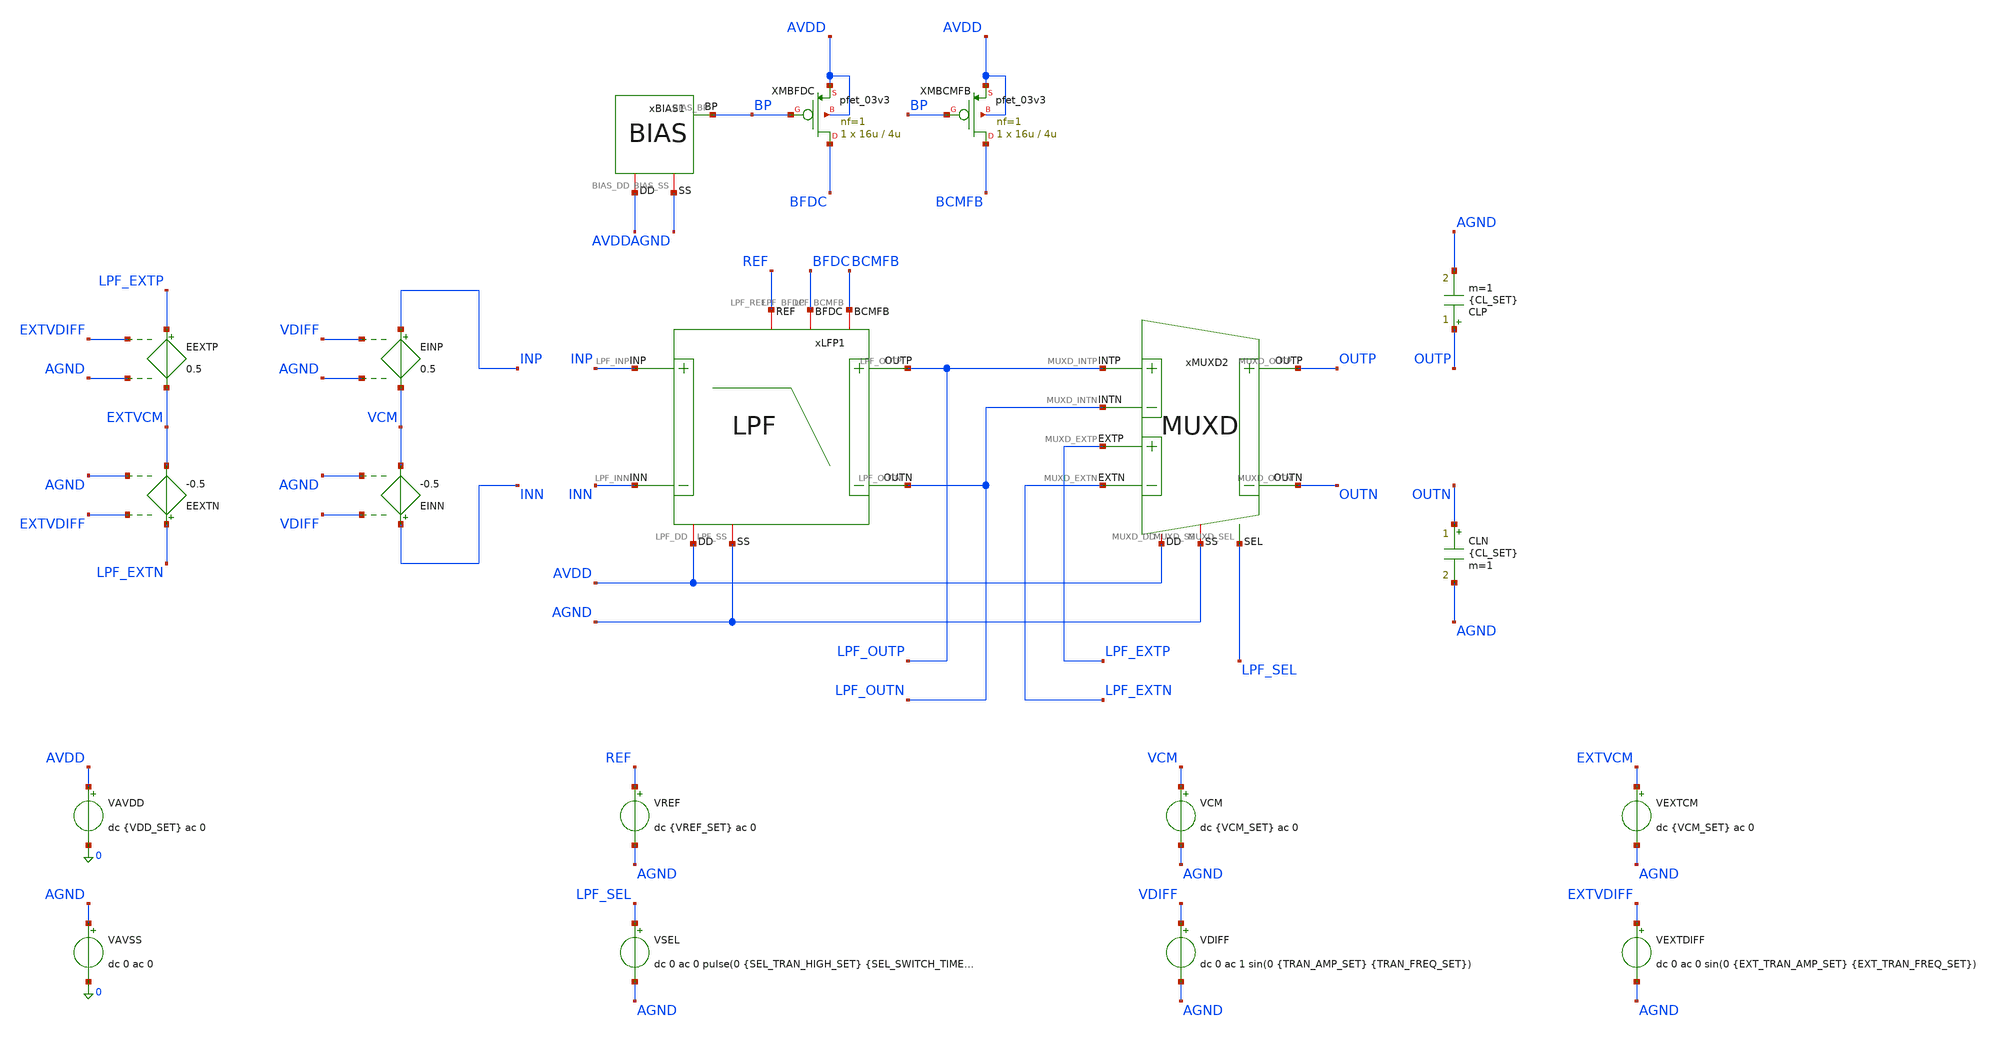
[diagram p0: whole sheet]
** sch_path: Design_Files/IC Design/Testbench/AFE_BLOCKS/LPF/LPF_TB_PVT_NOM.sch
**.subckt LPF_TB_PVT_NOM
CLP OUTP AGND {CL_SET} m=1
CLN OUTN AGND {CL_SET} m=1
xBIAS1 AVDD AGND BP BIAS
XMBFDC BFDC BP AVDD AVDD pfet_03v3 L=4u W=16u nf=1 ad='int((nf+1)/2) * W/nf * 0.18u' as='int((nf+2)/2) * W/nf * 0.18u'
+ pd='2*int((nf+1)/2) * (W/nf + 0.18u)' ps='2*int((nf+2)/2) * (W/nf + 0.18u)' nrd='0.18u / W' nrs='0.18u / W'
+ sa=0 sb=0 sd=0 m=1
XMBCMFB BCMFB BP AVDD AVDD pfet_03v3 L=4u W=16u nf=1 ad='int((nf+1)/2) * W/nf * 0.18u' as='int((nf+2)/2) * W/nf * 0.18u'
+ pd='2*int((nf+1)/2) * (W/nf + 0.18u)' ps='2*int((nf+2)/2) * (W/nf + 0.18u)' nrd='0.18u / W' nrs='0.18u / W'
+ sa=0 sb=0 sd=0 m=1
VAVDD AVDD 0 dc {VDD_SET} ac 0
.save i(vavdd)
VAVSS AGND 0 dc 0 ac 0
xLFP1 AVDD AGND INP INN LPF_OUTN BFDC LPF_OUTP BCMFB REF LPF
xMUXD2 AVDD AGND LPF_OUTP LPF_OUTN OUTN OUTP LPF_EXTP LPF_EXTN LPF_SEL MUXD
VCM VCM AGND dc {VCM_SET} ac 0
VDIFF VDIFF AGND dc 0 ac 1 sin(0 {TRAN_AMP_SET} {TRAN_FREQ_SET})
VREF REF AGND dc {VREF_SET} ac 0
VSEL LPF_SEL AGND dc 0 ac 0 pulse(0 {SEL_TRAN_HIGH_SET} {SEL_SWITCH_TIME_SET} 1u 1u 400m 800m)
VEXTCM EXTVCM AGND dc {VCM_SET} ac 0
VEXTDIFF EXTVDIFF AGND dc 0 ac 0 sin(0 {EXT_TRAN_AMP_SET} {EXT_TRAN_FREQ_SET})
EINP INP VCM VDIFF AGND 0.5
EINN INN VCM VDIFF AGND -0.5
EEXTP LPF_EXTP EXTVCM EXTVDIFF AGND 0.5
EEXTN LPF_EXTN EXTVCM EXTVDIFF AGND -0.5
**** begin user architecture code

* {MODELS_START}
.include $::180MCU_MODELS/design.ngspice

.param sw_stat_global=0
.param sw_stat_mismatch=0

.lib $::180MCU_MODELS/sm141064.ngspice typical
.lib $::180MCU_MODELS/sm141064.ngspice res_typical
.lib $::180MCU_MODELS/sm141064.ngspice mimcap_typical
.lib $::180MCU_MODELS/sm141064.ngspice cap_mim
.lib $::180MCU_MODELS/sm141064.ngspice bjt_typical

.csparam PROC_ID=0
* {MODELS_END}



* {SETUP_START}
.param VDD_SET=3.3
.param TEMP_SET=27

.param VCM_SET={VDD_SET/2}
.param VREF_SET={VDD_SET/2}

.param CL_SET=10p

.param LPF_GAIN_TARGET_SET=1
.param LPF_F1DB_TARGET_SET=150
.param LPF_F3DB_TARGET_SET=300

.param TRAN_AMP_SET=100m
.param TRAN_FREQ_SET=10

.param EXT_TRAN_AMP_SET=50m
.param EXT_TRAN_FREQ_SET=25

.param SEL_TRAN_HIGH_SET=0
.param SEL_SWITCH_TIME_SET=200m

.csparam MC_RUNS=200

.temp {TEMP_SET}

.options gmin=1e-12
.options rshunt=1e12
.options method=gear
* {SETUP_END}




* {MEAS_START}
.control

destroy all

set noaskquit
set wr_singlescale
unset wr_vecnames

option klu
option numdgt=15
option method=gear
option maxord=2
option plotwinsize=0

if $&PROC_ID = 0
set proc=NOM
else
if $&PROC_ID = 1
set proc=FF
else
if $&PROC_ID = 2
set proc=SS
else
if $&PROC_ID = 3
set proc=FS
else
set proc=SF
end
end
end
end

shell mkdir -p /foss/designs/ECG_Acquisition_IC/Measurement_Results/IC_Simulation/AFE_BLOCKS/LPF/{$proc}.Result_txt
shell rm -f /foss/designs/ECG_Acquisition_IC/Measurement_Results/IC_Simulation/AFE_BLOCKS/LPF/{$proc}.Result_txt/{$proc}.*.txt

foreach vddval 3.3 3.0 3.6
foreach tval 27 -40 125

if $vddval = 3.3
if $tval = 27
set env=nom
else
if $tval = -40
set env=tl
else
set env=th
end
end
else
if $vddval = 3.0
if $tval = 27
set env=vl
else
if $tval = -40
set env=vltl
else
set env=vlth
end
end
else
if $tval = 27
set env=vh
else
if $tval = -40
set env=vhtl
else
set env=vhth
end
end
end
end

alterparam VDD_SET=$vddval
alterparam TEMP_SET=$tval
alterparam SEL_TRAN_HIGH_SET=0
alterparam EXT_TRAN_AMP_SET=0

reset

save all
save @m.xmbfdc.m0[id]
save @m.xmbcmfb.m0[id]

* OFFSET

alter @VSEL[DC]=0
alter @VDIFF[DC]=0

alter @VDIFF[ACMAG]=0
alter @VCM[ACMAG]=0
alter @VREF[ACMAG]=0
alter @VEXTDIFF[ACMAG]=0
alter @VAVDD[ACMAG]=0
alter @VAVSS[ACMAG]=0

dc VDIFF -10m 10m 10u

let lpf_diff=v(LPF_OUTP)-v(LPF_OUTN)

meas dc vos_meas when lpf_diff=0 cross=1

set vos_val=$&vos_meas

echo $vos_val > /foss/designs/ECG_Acquisition_IC/Measurement_Results/IC_Simulation/AFE_BLOCKS/LPF/{$proc}.Result_txt/{$proc}.vos_{$env}.txt

destroy all

alter @VDIFF[DC]=$vos_val

* OP

op

let op_index=0

let vdd=v(AVDD)-v(AGND)
let vref=v(REF)-v(AGND)

let vin_cm=0.5*(v(INP)+v(INN))-v(AGND)
let vin_diff=v(INP)-v(INN)

let lpf_out_cm=0.5*(v(LPF_OUTP)+v(LPF_OUTN))-v(AGND)
let lpf_out_diff=v(LPF_OUTP)-v(LPF_OUTN)
let lpf_cm_error=lpf_out_cm-vref

let out_cm=0.5*(v(OUTP)+v(OUTN))-v(AGND)
let out_diff=v(OUTP)-v(OUTN)

let idd_total=abs(vavdd#branch)
let power_total=vdd*idd_total

let ibfdc=abs(@m.xmbfdc.m0[id])
let ibcmfb=abs(@m.xmbcmfb.m0[id])

setscale op_index

wrdata /foss/designs/ECG_Acquisition_IC/Measurement_Results/IC_Simulation/AFE_BLOCKS/LPF/{$proc}.Result_txt/{$proc}.op_{$env}.txt
+ vdd vref vin_cm vin_diff lpf_out_cm lpf_out_diff lpf_cm_error out_cm out_diff idd_total power_total ibfdc
+ ibcmfb

destroy all

* DIFF AC

alter @VDIFF[ACMAG]=1
alter @VCM[ACMAG]=0
alter @VREF[ACMAG]=0
alter @VEXTDIFF[ACMAG]=0
alter @VAVDD[ACMAG]=0
alter @VAVSS[ACMAG]=0

ac dec 200 0.01 100k

let vin_diff=v(INP)-v(INN)
let lpf_diff=v(LPF_OUTP)-v(LPF_OUTN)
let out_diff=v(OUTP)-v(OUTN)

let vin_r=real(vin_diff)
let vin_i=imag(vin_diff)
let lpf_r=real(lpf_diff)
let lpf_i=imag(lpf_diff)
let out_r=real(out_diff)
let out_i=imag(out_diff)

setscale frequency

wrdata /foss/designs/ECG_Acquisition_IC/Measurement_Results/IC_Simulation/AFE_BLOCKS/LPF/{$proc}.Result_txt/{$proc}.diff_ac_{$env}.txt
+ vin_r vin_i lpf_r lpf_i out_r out_i

destroy all

* CMRR

alter @VDIFF[ACMAG]=0
alter @VCM[ACMAG]=1
alter @VREF[ACMAG]=0
alter @VEXTDIFF[ACMAG]=0
alter @VAVDD[ACMAG]=0
alter @VAVSS[ACMAG]=0

ac dec 200 0.01 100k

let vin_cm=0.5*(v(INP)+v(INN))-v(AGND)
let lpf_diff=v(LPF_OUTP)-v(LPF_OUTN)

let vin_r=real(vin_cm)
let vin_i=imag(vin_cm)
let out_r=real(lpf_diff)
let out_i=imag(lpf_diff)

setscale frequency

wrdata /foss/designs/ECG_Acquisition_IC/Measurement_Results/IC_Simulation/AFE_BLOCKS/LPF/{$proc}.Result_txt/{$proc}.cmrr_ac_{$env}.txt
+ vin_r vin_i out_r out_i

destroy all

* PSRR+

alter @VDIFF[ACMAG]=0
alter @VCM[ACMAG]=0
alter @VREF[ACMAG]=0
alter @VEXTDIFF[ACMAG]=0
alter @VAVDD[ACMAG]=1
alter @VAVDD[ACPHASE]=0
alter @VAVSS[ACMAG]=0

ac dec 200 0.01 100k

let vsup=v(AVDD)-v(AGND)
let lpf_diff=v(LPF_OUTP)-v(LPF_OUTN)

let vsup_r=real(vsup)
let vsup_i=imag(vsup)
let out_r=real(lpf_diff)
let out_i=imag(lpf_diff)

setscale frequency

wrdata /foss/designs/ECG_Acquisition_IC/Measurement_Results/IC_Simulation/AFE_BLOCKS/LPF/{$proc}.Result_txt/{$proc}.psrrp_ac_{$env}.txt
+ vsup_r vsup_i out_r out_i

destroy all

* PSRR-

alter @VDIFF[ACMAG]=0
alter @VCM[ACMAG]=0
alter @VREF[ACMAG]=0
alter @VEXTDIFF[ACMAG]=0
alter @VAVDD[ACMAG]=0
alter @VAVSS[ACMAG]=1
alter @VAVSS[ACPHASE]=0

ac dec 200 0.01 100k

let vsup=v(AVDD)-v(AGND)
let lpf_diff=v(LPF_OUTP)-v(LPF_OUTN)

let vsup_r=real(vsup)
let vsup_i=imag(vsup)
let out_r=real(lpf_diff)
let out_i=imag(lpf_diff)

setscale frequency

wrdata /foss/designs/ECG_Acquisition_IC/Measurement_Results/IC_Simulation/AFE_BLOCKS/LPF/{$proc}.Result_txt/{$proc}.psrrn_ac_{$env}.txt
+ vsup_r vsup_i out_r out_i

destroy all

* NOISE

alter @VDIFF[ACMAG]=1
alter @VCM[ACMAG]=0
alter @VREF[ACMAG]=0
alter @VEXTDIFF[ACMAG]=0
alter @VAVDD[ACMAG]=0
alter @VAVSS[ACMAG]=0

noise v(LPF_OUTP,LPF_OUTN) VDIFF dec 100 0.01 10k

setplot previous
setscale frequency

wrdata /foss/designs/ECG_Acquisition_IC/Measurement_Results/IC_Simulation/AFE_BLOCKS/LPF/{$proc}.Result_txt/{$proc}.noise_{$env}.txt
+ onoise_spectrum inoise_spectrum

destroy all


* LPF VTC

alter @VSEL[DC]=0
alter @VDIFF[DC]=0

alter @VDIFF[ACMAG]=0
alter @VCM[ACMAG]=0
alter @VREF[ACMAG]=0
alter @VEXTDIFF[ACMAG]=0
alter @VAVDD[ACMAG]=0
alter @VAVSS[ACMAG]=0

if $vddval = 3.0
dc VDIFF -3.0 3.0 6m
end

if $vddval = 3.3
dc VDIFF -3.3 3.3 6.6m
end

if $vddval = 3.6
dc VDIFF -3.6 3.6 7.2m
end

let vin_diff=v(INP)-v(INN)
let lpf_outp=v(LPF_OUTP)-v(AGND)
let lpf_outn=v(LPF_OUTN)-v(AGND)
let lpf_out_cm=0.5*(v(LPF_OUTP)+v(LPF_OUTN))-v(AGND)
let lpf_out_diff=v(LPF_OUTP)-v(LPF_OUTN)

wrdata /foss/designs/ECG_Acquisition_IC/Measurement_Results/IC_Simulation/AFE_BLOCKS/LPF/{$proc}.Result_txt/{$proc}.vtc_{$env}.txt
+ vin_diff lpf_outp lpf_outn lpf_out_cm lpf_out_diff

destroy all


* LPF THD

* 5 mVpp ECG x INA gain 240 = 1.2 Vpp = 0.6 V peak.
alterparam TRAN_AMP_SET=0.6
alterparam TRAN_FREQ_SET=60

reset

save v(INP) v(INN)
save v(LPF_OUTP) v(LPF_OUTN)

alter @VSEL[DC]=0
alter @VDIFF[DC]=0

alter @VDIFF[ACMAG]=0
alter @VCM[ACMAG]=0
alter @VREF[ACMAG]=0
alter @VEXTDIFF[ACMAG]=0
alter @VAVDD[ACMAG]=0
alter @VAVSS[ACMAG]=0

* 100 ms settling and 10 measured cycles.
tran 50u 266.666667m 100m

let vin_diff=v(INP)-v(INN)
let lpf_out_diff=v(LPF_OUTP)-v(LPF_OUTN)

wrdata /foss/designs/ECG_Acquisition_IC/Measurement_Results/IC_Simulation/AFE_BLOCKS/LPF/{$proc}.Result_txt/{$proc}.thd_{$env}.txt
+ vin_diff lpf_out_diff

destroy all

alterparam TRAN_AMP_SET=100m
alterparam TRAN_FREQ_SET=10


end
end

* SEL

if $&PROC_ID = 0

alterparam VDD_SET=3.3
alterparam TEMP_SET=27

alterparam TRAN_AMP_SET=100m
alterparam TRAN_FREQ_SET=10

alterparam EXT_TRAN_AMP_SET=50m
alterparam EXT_TRAN_FREQ_SET=25

alterparam SEL_TRAN_HIGH_SET=3.3
alterparam SEL_SWITCH_TIME_SET=200m

reset

save all

tran 20u 400m

let int_in_diff=v(INP)-v(INN)
let ext_diff=v(LPF_EXTP)-v(LPF_EXTN)
let out_diff=v(OUTP)-v(OUTN)

wrdata /foss/designs/ECG_Acquisition_IC/Measurement_Results/IC_Simulation/AFE_BLOCKS/LPF/{$proc}.Result_txt/{$proc}.sel_tran_nom.txt
+ v(LPF_SEL) int_in_diff ext_diff out_diff

destroy all

end

quit

.endc
* {MEAS_END}


**** end user architecture code
**.ends
.end
